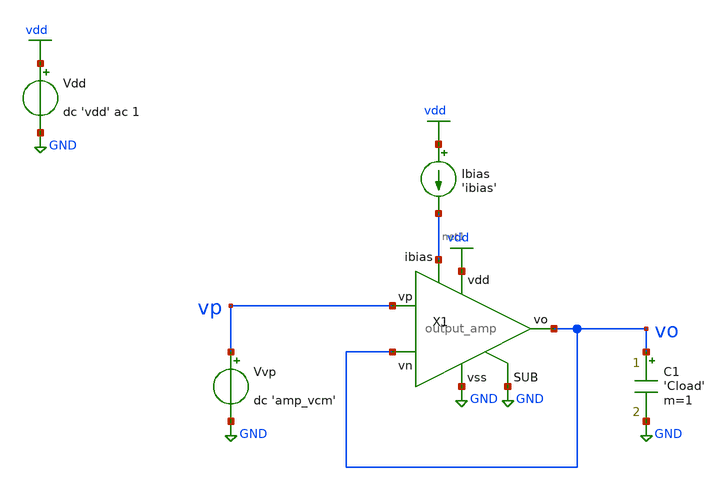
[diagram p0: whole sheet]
** sch_path: tb/output_amp/tb_amp_psrr.sch
**.subckt tb_amp_psrr
X1 vdd vo vp vo net1 GND GND output_amp
Vdd vdd GND dc 'vdd' ac 1
Vvp vp GND dc 'amp_vcm'
Ibias vdd net1 'ibias'
C1 vo GND 'Cload' m=1
**** begin user architecture code


.lib 'models_dir'/cornerMOShv.lib 'mos_corner'
.lib 'models_dir'/cornerCAP.lib cap_typ
.option TEMP='temperature'
.option warn=1
.control
save all
ac dec 20 'frequency_start' 'frequency_stop'
set wr_singlescale
wrdata 'simpath'/'filename'_'N'.data vdb(vo)
quit
.endc


**** end user architecture code
**.ends
.GLOBAL GND
.GLOBAL vdd
.end
